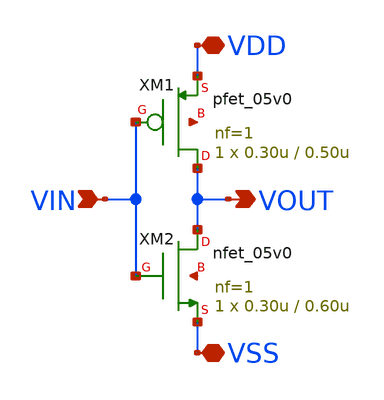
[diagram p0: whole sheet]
** sch_path: week01_mosfet_cmos/tugas2_cmos_inverter/cmos-inverter3.sch
**.subckt cmos-inverter3 VDD VSS VIN VOUT
*.iopin VDD
*.iopin VSS
*.ipin VIN
*.opin VOUT
XM1 VOUT VIN VDD net1 pfet_05v0 L=0.50u W=0.30u nf=1 ad='int((nf+1)/2) * W/nf * 0.18u' as='int((nf+2)/2) * W/nf * 0.18u'
+ pd='2*int((nf+1)/2) * (W/nf + 0.18u)' ps='2*int((nf+2)/2) * (W/nf + 0.18u)' nrd='0.18u / W' nrs='0.18u / W'
+ sa=0 sb=0 sd=0 m=1
XM2 VOUT VIN VSS net2 nfet_05v0 L=0.60u W=0.30u nf=1 ad='int((nf+1)/2) * W/nf * 0.18u' as='int((nf+2)/2) * W/nf * 0.18u'
+ pd='2*int((nf+1)/2) * (W/nf + 0.18u)' ps='2*int((nf+2)/2) * (W/nf + 0.18u)' nrd='0.18u / W' nrs='0.18u / W'
+ sa=0 sb=0 sd=0 m=1
**.ends
.end
